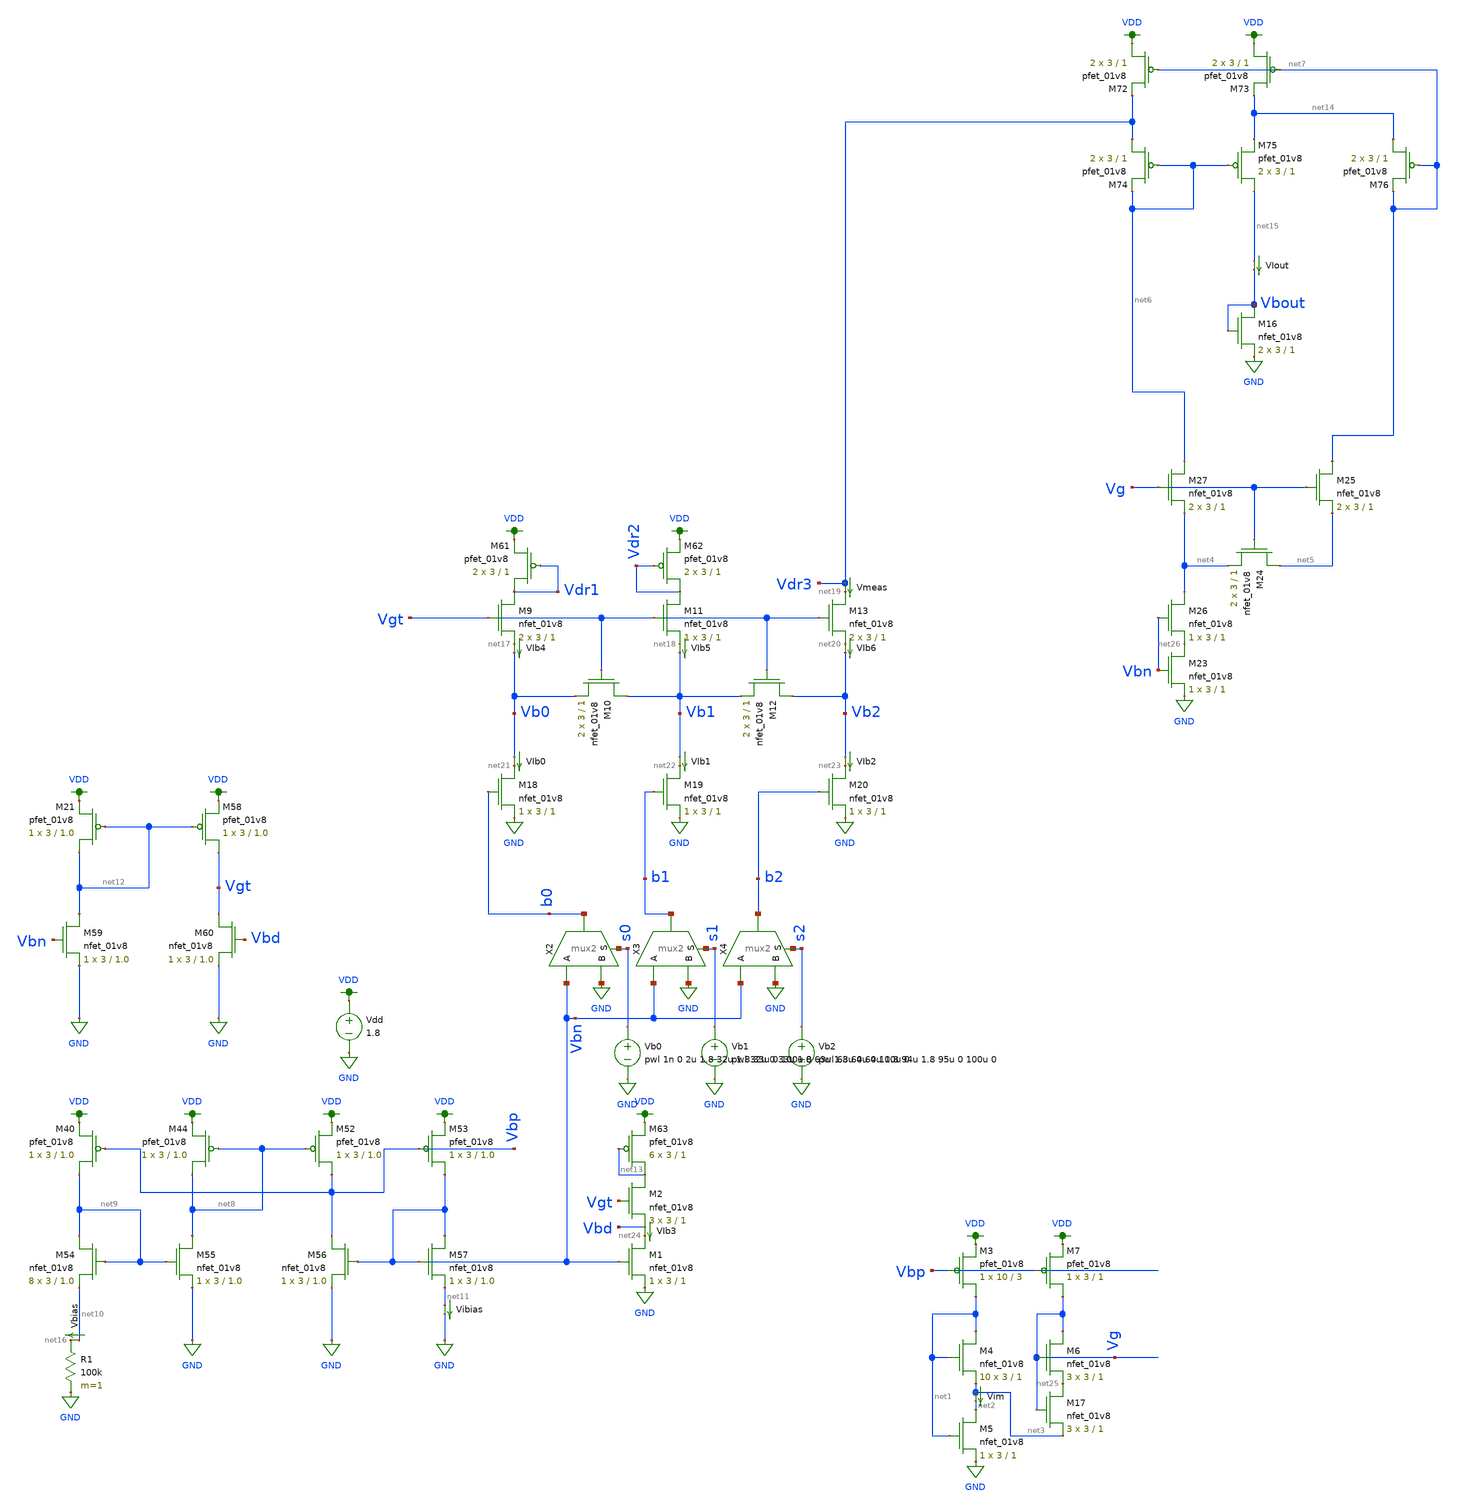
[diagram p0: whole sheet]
** sch_path: schematic/archive/ladder3_test_josh_wilson_dynamic_nomirror.sch
**.subckt ladder3_test_josh_wilson_dynamic_nomirror
X2 b0 Vbn GND s0 mux2
X3 b1 Vbn GND s1 mux2
X4 b2 Vbn GND s2 mux2
R1 net16 GND 100k m=1
Vdd VDD GND 1.8
Vb0 s0 GND pwl 1n 0 2u 1.8 32u 1.8 33u 0 100u 0
Vb1 s1 GND pwl 32u 0 33u 1.8 63u 1.8 64u 0 100u 0
Vb2 s2 GND pwl 63u 0 64u 1.8 94u 1.8 95u 0 100u 0
XM9 Vdr1 Vgt net17 GND sky130_fd_pr__nfet_01v8 L=1 W=3 nf=1 ad='int((nf+1)/2) * W/nf * 0.29' as='int((nf+2)/2) * W/nf * 0.29'
+ pd='2*int((nf+1)/2) * (W/nf + 0.29)' ps='2*int((nf+2)/2) * (W/nf + 0.29)' nrd='0.29 / W' nrs='0.29 / W'
+ sa=0 sb=0 sd=0 mult=2 m=2
XM10 Vb1 Vgt Vb0 GND sky130_fd_pr__nfet_01v8 L=1 W=3 nf=1 ad='int((nf+1)/2) * W/nf * 0.29' as='int((nf+2)/2) * W/nf * 0.29'
+ pd='2*int((nf+1)/2) * (W/nf + 0.29)' ps='2*int((nf+2)/2) * (W/nf + 0.29)' nrd='0.29 / W' nrs='0.29 / W'
+ sa=0 sb=0 sd=0 mult=2 m=2
XM11 Vdr2 Vgt net18 GND sky130_fd_pr__nfet_01v8 L=1 W=3 nf=1 ad='int((nf+1)/2) * W/nf * 0.29' as='int((nf+2)/2) * W/nf * 0.29'
+ pd='2*int((nf+1)/2) * (W/nf + 0.29)' ps='2*int((nf+2)/2) * (W/nf + 0.29)' nrd='0.29 / W' nrs='0.29 / W'
+ sa=0 sb=0 sd=0 mult=1 m=1
XM12 Vb2 Vgt Vb1 GND sky130_fd_pr__nfet_01v8 L=1 W=3 nf=1 ad='int((nf+1)/2) * W/nf * 0.29' as='int((nf+2)/2) * W/nf * 0.29'
+ pd='2*int((nf+1)/2) * (W/nf + 0.29)' ps='2*int((nf+2)/2) * (W/nf + 0.29)' nrd='0.29 / W' nrs='0.29 / W'
+ sa=0 sb=0 sd=0 mult=2 m=2
XM13 net19 Vgt net20 GND sky130_fd_pr__nfet_01v8 L=1 W=3 nf=1 ad='int((nf+1)/2) * W/nf * 0.29' as='int((nf+2)/2) * W/nf * 0.29'
+ pd='2*int((nf+1)/2) * (W/nf + 0.29)' ps='2*int((nf+2)/2) * (W/nf + 0.29)' nrd='0.29 / W' nrs='0.29 / W'
+ sa=0 sb=0 sd=0 mult=2 m=2
XM18 net21 b0 GND GND sky130_fd_pr__nfet_01v8 L=1 W=3 nf=1 ad='int((nf+1)/2) * W/nf * 0.29' as='int((nf+2)/2) * W/nf * 0.29'
+ pd='2*int((nf+1)/2) * (W/nf + 0.29)' ps='2*int((nf+2)/2) * (W/nf + 0.29)' nrd='0.29 / W' nrs='0.29 / W'
+ sa=0 sb=0 sd=0 mult=1 m=1
XM19 net22 b1 GND GND sky130_fd_pr__nfet_01v8 L=1 W=3 nf=1 ad='int((nf+1)/2) * W/nf * 0.29' as='int((nf+2)/2) * W/nf * 0.29'
+ pd='2*int((nf+1)/2) * (W/nf + 0.29)' ps='2*int((nf+2)/2) * (W/nf + 0.29)' nrd='0.29 / W' nrs='0.29 / W'
+ sa=0 sb=0 sd=0 mult=1 m=1
XM20 net23 b2 GND GND sky130_fd_pr__nfet_01v8 L=1 W=3 nf=1 ad='int((nf+1)/2) * W/nf * 0.29' as='int((nf+2)/2) * W/nf * 0.29'
+ pd='2*int((nf+1)/2) * (W/nf + 0.29)' ps='2*int((nf+2)/2) * (W/nf + 0.29)' nrd='0.29 / W' nrs='0.29 / W'
+ sa=0 sb=0 sd=0 mult=1 m=1
Vmeas Vdr3 net19 0
.save i(vmeas)
Vbias net10 net16 0
.save i(vbias)
VIb0 Vb0 net21 0
.save i(vib0)
VIb1 Vb1 net22 0
.save i(vib1)
VIb2 Vb2 net23 0
.save i(vib2)
XM1 net24 Vbn GND GND sky130_fd_pr__nfet_01v8 L=1 W=3 nf=1 ad='int((nf+1)/2) * W/nf * 0.29' as='int((nf+2)/2) * W/nf * 0.29'
+ pd='2*int((nf+1)/2) * (W/nf + 0.29)' ps='2*int((nf+2)/2) * (W/nf + 0.29)' nrd='0.29 / W' nrs='0.29 / W'
+ sa=0 sb=0 sd=0 mult=1 m=1
VIb3 Vbd net24 0
.save i(vib3)
XM3 net1 Vbp VDD VDD sky130_fd_pr__pfet_01v8 L=3 W=10 nf=1 ad='int((nf+1)/2) * W/nf * 0.29' as='int((nf+2)/2) * W/nf * 0.29'
+ pd='2*int((nf+1)/2) * (W/nf + 0.29)' ps='2*int((nf+2)/2) * (W/nf + 0.29)' nrd='0.29 / W' nrs='0.29 / W'
+ sa=0 sb=0 sd=0 mult=1 m=1
XM4 net1 net1 net3 GND sky130_fd_pr__nfet_01v8 L=1 W=3 nf=1 ad='int((nf+1)/2) * W/nf * 0.29' as='int((nf+2)/2) * W/nf * 0.29'
+ pd='2*int((nf+1)/2) * (W/nf + 0.29)' ps='2*int((nf+2)/2) * (W/nf + 0.29)' nrd='0.29 / W' nrs='0.29 / W'
+ sa=0 sb=0 sd=0 mult=10 m=10
XM5 net2 net1 GND GND sky130_fd_pr__nfet_01v8 L=1 W=3 nf=1 ad='int((nf+1)/2) * W/nf * 0.29' as='int((nf+2)/2) * W/nf * 0.29'
+ pd='2*int((nf+1)/2) * (W/nf + 0.29)' ps='2*int((nf+2)/2) * (W/nf + 0.29)' nrd='0.29 / W' nrs='0.29 / W'
+ sa=0 sb=0 sd=0 mult=1 m=1
Vim net3 net2 0
.save i(vim)
XM6 Vg Vg net25 GND sky130_fd_pr__nfet_01v8 L=1 W=3 nf=1 ad='int((nf+1)/2) * W/nf * 0.29' as='int((nf+2)/2) * W/nf * 0.29'
+ pd='2*int((nf+1)/2) * (W/nf + 0.29)' ps='2*int((nf+2)/2) * (W/nf + 0.29)' nrd='0.29 / W' nrs='0.29 / W'
+ sa=0 sb=0 sd=0 mult=3 m=3
XM7 Vg Vbp VDD VDD sky130_fd_pr__pfet_01v8 L=1 W=3 nf=1 ad='int((nf+1)/2) * W/nf * 0.29' as='int((nf+2)/2) * W/nf * 0.29'
+ pd='2*int((nf+1)/2) * (W/nf + 0.29)' ps='2*int((nf+2)/2) * (W/nf + 0.29)' nrd='0.29 / W' nrs='0.29 / W'
+ sa=0 sb=0 sd=0 mult=1 m=1
VIb4 net17 Vb0 0
.save i(vib4)
VIb5 net18 Vb1 0
.save i(vib5)
VIb6 net20 Vb2 0
.save i(vib6)
VIout net15 Vbout 0
.save i(viout)
XM24 net5 Vg net4 GND sky130_fd_pr__nfet_01v8 L=1 W=3 nf=1 ad='int((nf+1)/2) * W/nf * 0.29' as='int((nf+2)/2) * W/nf * 0.29'
+ pd='2*int((nf+1)/2) * (W/nf + 0.29)' ps='2*int((nf+2)/2) * (W/nf + 0.29)' nrd='0.29 / W' nrs='0.29 / W'
+ sa=0 sb=0 sd=0 mult=2 m=2
XM25 net7 Vg net5 GND sky130_fd_pr__nfet_01v8 L=1 W=3 nf=1 ad='int((nf+1)/2) * W/nf * 0.29' as='int((nf+2)/2) * W/nf * 0.29'
+ pd='2*int((nf+1)/2) * (W/nf + 0.29)' ps='2*int((nf+2)/2) * (W/nf + 0.29)' nrd='0.29 / W' nrs='0.29 / W'
+ sa=0 sb=0 sd=0 mult=2 m=2
XM26 net4 Vbn net26 GND sky130_fd_pr__nfet_01v8 L=1 W=3 nf=1 ad='int((nf+1)/2) * W/nf * 0.29' as='int((nf+2)/2) * W/nf * 0.29'
+ pd='2*int((nf+1)/2) * (W/nf + 0.29)' ps='2*int((nf+2)/2) * (W/nf + 0.29)' nrd='0.29 / W' nrs='0.29 / W'
+ sa=0 sb=0 sd=0 mult=1 m=1
XM27 net6 Vg net4 GND sky130_fd_pr__nfet_01v8 L=1 W=3 nf=1 ad='int((nf+1)/2) * W/nf * 0.29' as='int((nf+2)/2) * W/nf * 0.29'
+ pd='2*int((nf+1)/2) * (W/nf + 0.29)' ps='2*int((nf+2)/2) * (W/nf + 0.29)' nrd='0.29 / W' nrs='0.29 / W'
+ sa=0 sb=0 sd=0 mult=2 m=2
XM16 Vbout Vbout GND GND sky130_fd_pr__nfet_01v8 L=1 W=3 nf=1 ad='int((nf+1)/2) * W/nf * 0.29' as='int((nf+2)/2) * W/nf * 0.29'
+ pd='2*int((nf+1)/2) * (W/nf + 0.29)' ps='2*int((nf+2)/2) * (W/nf + 0.29)' nrd='0.29 / W' nrs='0.29 / W'
+ sa=0 sb=0 sd=0 mult=2 m=2
XM40 net9 Vbp VDD VDD sky130_fd_pr__pfet_01v8 L=1.0 W=3 nf=1 ad='int((nf+1)/2) * W/nf * 0.29' as='int((nf+2)/2) * W/nf * 0.29'
+ pd='2*int((nf+1)/2) * (W/nf + 0.29)' ps='2*int((nf+2)/2) * (W/nf + 0.29)' nrd='0.29 / W' nrs='0.29 / W'
+ sa=0 sb=0 sd=0 mult=1 m=1
XM44 net8 net8 VDD VDD sky130_fd_pr__pfet_01v8 L=1.0 W=3 nf=1 ad='int((nf+1)/2) * W/nf * 0.29' as='int((nf+2)/2) * W/nf * 0.29'
+ pd='2*int((nf+1)/2) * (W/nf + 0.29)' ps='2*int((nf+2)/2) * (W/nf + 0.29)' nrd='0.29 / W' nrs='0.29 / W'
+ sa=0 sb=0 sd=0 mult=1 m=1
XM52 Vbp net8 VDD VDD sky130_fd_pr__pfet_01v8 L=1.0 W=3 nf=1 ad='int((nf+1)/2) * W/nf * 0.29' as='int((nf+2)/2) * W/nf * 0.29'
+ pd='2*int((nf+1)/2) * (W/nf + 0.29)' ps='2*int((nf+2)/2) * (W/nf + 0.29)' nrd='0.29 / W' nrs='0.29 / W'
+ sa=0 sb=0 sd=0 mult=1 m=1
XM53 Vbn Vbp VDD VDD sky130_fd_pr__pfet_01v8 L=1.0 W=3 nf=1 ad='int((nf+1)/2) * W/nf * 0.29' as='int((nf+2)/2) * W/nf * 0.29'
+ pd='2*int((nf+1)/2) * (W/nf + 0.29)' ps='2*int((nf+2)/2) * (W/nf + 0.29)' nrd='0.29 / W' nrs='0.29 / W'
+ sa=0 sb=0 sd=0 mult=1 m=1
XM54 net9 net9 net10 GND sky130_fd_pr__nfet_01v8 L=1.0 W=3 nf=1 ad='int((nf+1)/2) * W/nf * 0.29' as='int((nf+2)/2) * W/nf * 0.29'
+ pd='2*int((nf+1)/2) * (W/nf + 0.29)' ps='2*int((nf+2)/2) * (W/nf + 0.29)' nrd='0.29 / W' nrs='0.29 / W'
+ sa=0 sb=0 sd=0 mult=8 m=8
XM55 net8 net9 GND GND sky130_fd_pr__nfet_01v8 L=1.0 W=3 nf=1 ad='int((nf+1)/2) * W/nf * 0.29' as='int((nf+2)/2) * W/nf * 0.29'
+ pd='2*int((nf+1)/2) * (W/nf + 0.29)' ps='2*int((nf+2)/2) * (W/nf + 0.29)' nrd='0.29 / W' nrs='0.29 / W'
+ sa=0 sb=0 sd=0 mult=1 m=1
XM56 Vbp Vbn GND GND sky130_fd_pr__nfet_01v8 L=1.0 W=3 nf=1 ad='int((nf+1)/2) * W/nf * 0.29' as='int((nf+2)/2) * W/nf * 0.29'
+ pd='2*int((nf+1)/2) * (W/nf + 0.29)' ps='2*int((nf+2)/2) * (W/nf + 0.29)' nrd='0.29 / W' nrs='0.29 / W'
+ sa=0 sb=0 sd=0 mult=1 m=1
XM57 Vbn Vbn net11 GND sky130_fd_pr__nfet_01v8 L=1.0 W=3 nf=1 ad='int((nf+1)/2) * W/nf * 0.29' as='int((nf+2)/2) * W/nf * 0.29'
+ pd='2*int((nf+1)/2) * (W/nf + 0.29)' ps='2*int((nf+2)/2) * (W/nf + 0.29)' nrd='0.29 / W' nrs='0.29 / W'
+ sa=0 sb=0 sd=0 mult=1 m=1
Vibias net11 GND 0
.save i(vibias)
XM2 net13 Vgt Vbd GND sky130_fd_pr__nfet_01v8 L=1 W=3 nf=1 ad='int((nf+1)/2) * W/nf * 0.29' as='int((nf+2)/2) * W/nf * 0.29'
+ pd='2*int((nf+1)/2) * (W/nf + 0.29)' ps='2*int((nf+2)/2) * (W/nf + 0.29)' nrd='0.29 / W' nrs='0.29 / W'
+ sa=0 sb=0 sd=0 mult=3 m=3
XM17 net25 Vg net3 GND sky130_fd_pr__nfet_01v8 L=1 W=3 nf=1 ad='int((nf+1)/2) * W/nf * 0.29' as='int((nf+2)/2) * W/nf * 0.29'
+ pd='2*int((nf+1)/2) * (W/nf + 0.29)' ps='2*int((nf+2)/2) * (W/nf + 0.29)' nrd='0.29 / W' nrs='0.29 / W'
+ sa=0 sb=0 sd=0 mult=3 m=3
XM21 net12 net12 VDD VDD sky130_fd_pr__pfet_01v8 L=1.0 W=3 nf=1 ad='int((nf+1)/2) * W/nf * 0.29' as='int((nf+2)/2) * W/nf * 0.29'
+ pd='2*int((nf+1)/2) * (W/nf + 0.29)' ps='2*int((nf+2)/2) * (W/nf + 0.29)' nrd='0.29 / W' nrs='0.29 / W'
+ sa=0 sb=0 sd=0 mult=1 m=1
XM58 Vgt net12 VDD VDD sky130_fd_pr__pfet_01v8 L=1.0 W=3 nf=1 ad='int((nf+1)/2) * W/nf * 0.29' as='int((nf+2)/2) * W/nf * 0.29'
+ pd='2*int((nf+1)/2) * (W/nf + 0.29)' ps='2*int((nf+2)/2) * (W/nf + 0.29)' nrd='0.29 / W' nrs='0.29 / W'
+ sa=0 sb=0 sd=0 mult=1 m=1
XM59 net12 Vbn GND GND sky130_fd_pr__nfet_01v8 L=1.0 W=3 nf=1 ad='int((nf+1)/2) * W/nf * 0.29' as='int((nf+2)/2) * W/nf * 0.29'
+ pd='2*int((nf+1)/2) * (W/nf + 0.29)' ps='2*int((nf+2)/2) * (W/nf + 0.29)' nrd='0.29 / W' nrs='0.29 / W'
+ sa=0 sb=0 sd=0 mult=1 m=1
XM60 Vgt Vbd GND GND sky130_fd_pr__nfet_01v8 L=1.0 W=3 nf=1 ad='int((nf+1)/2) * W/nf * 0.29' as='int((nf+2)/2) * W/nf * 0.29'
+ pd='2*int((nf+1)/2) * (W/nf + 0.29)' ps='2*int((nf+2)/2) * (W/nf + 0.29)' nrd='0.29 / W' nrs='0.29 / W'
+ sa=0 sb=0 sd=0 mult=1 m=1
XM61 Vdr1 Vdr1 VDD VDD sky130_fd_pr__pfet_01v8 L=1 W=3 nf=1 ad='int((nf+1)/2) * W/nf * 0.29' as='int((nf+2)/2) * W/nf * 0.29'
+ pd='2*int((nf+1)/2) * (W/nf + 0.29)' ps='2*int((nf+2)/2) * (W/nf + 0.29)' nrd='0.29 / W' nrs='0.29 / W'
+ sa=0 sb=0 sd=0 mult=2 m=2
XM62 Vdr2 Vdr2 VDD VDD sky130_fd_pr__pfet_01v8 L=1 W=3 nf=1 ad='int((nf+1)/2) * W/nf * 0.29' as='int((nf+2)/2) * W/nf * 0.29'
+ pd='2*int((nf+1)/2) * (W/nf + 0.29)' ps='2*int((nf+2)/2) * (W/nf + 0.29)' nrd='0.29 / W' nrs='0.29 / W'
+ sa=0 sb=0 sd=0 mult=2 m=2
XM63 net13 net13 VDD VDD sky130_fd_pr__pfet_01v8 L=1 W=3 nf=1 ad='int((nf+1)/2) * W/nf * 0.29' as='int((nf+2)/2) * W/nf * 0.29'
+ pd='2*int((nf+1)/2) * (W/nf + 0.29)' ps='2*int((nf+2)/2) * (W/nf + 0.29)' nrd='0.29 / W' nrs='0.29 / W'
+ sa=0 sb=0 sd=0 mult=6 m=6
XM72 VDD net7 Vdr3 VDD sky130_fd_pr__pfet_01v8 L=1 W=3 nf=1 ad='int((nf+1)/2) * W/nf * 0.29' as='int((nf+2)/2) * W/nf * 0.29'
+ pd='2*int((nf+1)/2) * (W/nf + 0.29)' ps='2*int((nf+2)/2) * (W/nf + 0.29)' nrd='0.29 / W' nrs='0.29 / W'
+ sa=0 sb=0 sd=0 mult=2 m=2
XM73 VDD net7 net14 VDD sky130_fd_pr__pfet_01v8 L=1 W=3 nf=1 ad='int((nf+1)/2) * W/nf * 0.29' as='int((nf+2)/2) * W/nf * 0.29'
+ pd='2*int((nf+1)/2) * (W/nf + 0.29)' ps='2*int((nf+2)/2) * (W/nf + 0.29)' nrd='0.29 / W' nrs='0.29 / W'
+ sa=0 sb=0 sd=0 mult=2 m=2
XM74 Vdr3 net6 net6 VDD sky130_fd_pr__pfet_01v8 L=1 W=3 nf=1 ad='int((nf+1)/2) * W/nf * 0.29' as='int((nf+2)/2) * W/nf * 0.29'
+ pd='2*int((nf+1)/2) * (W/nf + 0.29)' ps='2*int((nf+2)/2) * (W/nf + 0.29)' nrd='0.29 / W' nrs='0.29 / W'
+ sa=0 sb=0 sd=0 mult=2 m=2
XM75 net15 net6 net14 VDD sky130_fd_pr__pfet_01v8 L=1 W=3 nf=1 ad='int((nf+1)/2) * W/nf * 0.29' as='int((nf+2)/2) * W/nf * 0.29'
+ pd='2*int((nf+1)/2) * (W/nf + 0.29)' ps='2*int((nf+2)/2) * (W/nf + 0.29)' nrd='0.29 / W' nrs='0.29 / W'
+ sa=0 sb=0 sd=0 mult=2 m=2
XM76 net14 net7 net7 VDD sky130_fd_pr__pfet_01v8 L=1 W=3 nf=1 ad='int((nf+1)/2) * W/nf * 0.29' as='int((nf+2)/2) * W/nf * 0.29'
+ pd='2*int((nf+1)/2) * (W/nf + 0.29)' ps='2*int((nf+2)/2) * (W/nf + 0.29)' nrd='0.29 / W' nrs='0.29 / W'
+ sa=0 sb=0 sd=0 mult=2 m=2
XM23 net26 Vbn GND GND sky130_fd_pr__nfet_01v8 L=1 W=3 nf=1 ad='int((nf+1)/2) * W/nf * 0.29' as='int((nf+2)/2) * W/nf * 0.29'
+ pd='2*int((nf+1)/2) * (W/nf + 0.29)' ps='2*int((nf+2)/2) * (W/nf + 0.29)' nrd='0.29 / W' nrs='0.29 / W'
+ sa=0 sb=0 sd=0 mult=1 m=1
**** begin user architecture code

.option wnflag=1
.param MC_SWITCH=0.0
.lib ~/skywater/skywater-pdk/libraries/sky130_fd_pr_ngspice/latest/models/sky130.lib.spice tt


.control
tran 0.01u 100u
run
plot tran1.i(Vmeas) tran1.i(Vbias) tran1.i(VIb3) tran1.i(VIout)
plot tran1.i(Vib0) tran1.i(Vib1) tran1.i(Vib2)
*plot tran1.v(b0) tran1.v(b1) tran1.v(b2) tran1.v(vbn)
*plot tran1.v(Vdr1) tran1.v(Vdr2) tran1.v(Vdr3)
plot tran1.v(Vbn) tran1.v(Vb0) tran1.v(Vb1) tran1.v(Vb2) tran1.v(Vbd)
plot tran1.i(VIout) tran1.i(Vmeas)
*plot tran1.i(Vib4) tran1.i(Vib5) tran1.i(Vib6)
*plot tran1.v(s0) tran1.v(s1) tran1.v(s2)
*plot tran1.v(Vdr1) tran1.v(Vdr2) tran1.v(Vdr3) tran1.v(Vdr4) tran1.v(Vdr5)
reset
*dc Vdd 0 1.8 0.01
*plot dc.i(Vmeas) dc.i(Vbias) dc.i(VIb3) dc.i(VIout)
*plot dc.v(Vdr3) dc.v(Vbout)
.endc
.save all

**** end user architecture code
**.ends
.GLOBAL GND
.GLOBAL VDD
.end
